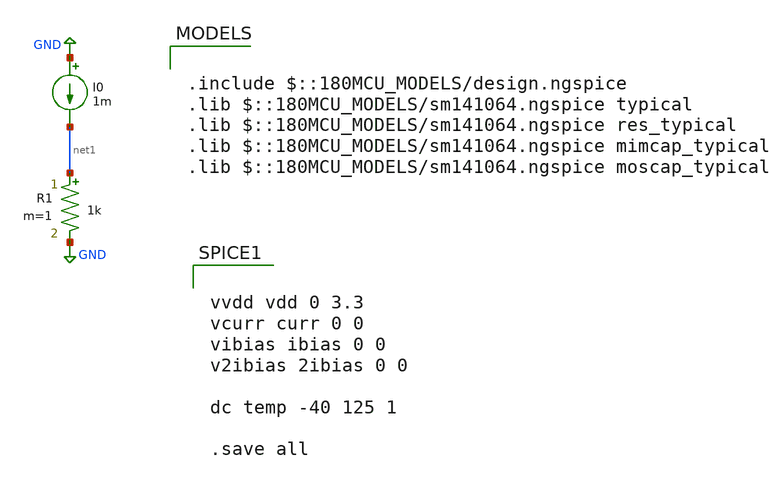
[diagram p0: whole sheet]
** sch_path: Clock_Reference/symbols/untitled-2.sch
**.subckt untitled-2
I0 GND net1 1m
R1 net1 GND 1k m=1
**** begin user architecture code

.include $::180MCU_MODELS/design.ngspice
.lib $::180MCU_MODELS/sm141064.ngspice typical
.lib $::180MCU_MODELS/sm141064.ngspice res_typical
.lib $::180MCU_MODELS/sm141064.ngspice mimcap_typical
.lib $::180MCU_MODELS/sm141064.ngspice moscap_typical



vvdd vdd 0 3.3
vcurr curr 0 0
vibias ibias 0 0
v2ibias 2ibias 0 0

dc temp -40 125 1

.save all


**** end user architecture code
**.ends
.GLOBAL GND
.end
